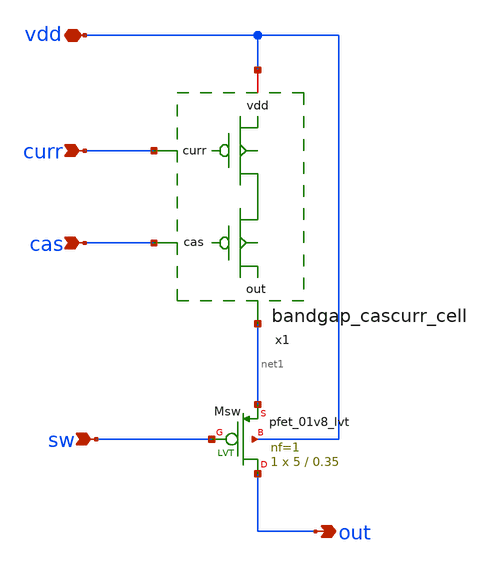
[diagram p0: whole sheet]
** sch_path: design/bandgap_cascurr_cell_sw/bandgap_cascurr_cell_sw.sch
**.subckt bandgap_cascurr_cell_sw vdd curr cas out sw
*.iopin vdd
*.ipin curr
*.ipin cas
*.opin out
*.ipin sw
x1 vdd curr cas net1 bandgap_cascurr_cell m=1
XMsw out sw net1 vdd sky130_fd_pr__pfet_01v8_lvt L=0.35 W=5 nf=1 ad='W * 0.29' as='W * 0.29' pd='2 * (W + 0.29)'
+ ps='2 * (W + 0.29)' nrd='0.29 / W' nrs='0.29 / W' sa=0 sb=0 sd=0 mult=1 m=1
**.ends

* expanding   symbol:  bandgap_cascurr_cell/bandgap_cascurr_cell.sym # of pins=4
** sym_path: design/bandgap_cascurr_cell/bandgap_cascurr_cell.sym
** sch_path: design/bandgap_cascurr_cell/bandgap_cascurr_cell.sch
.subckt bandgap_cascurr_cell vdd curr cas out
*.iopin vdd
*.ipin curr
*.ipin cas
*.opin out
XMcurr net1 curr vdd vdd sky130_fd_pr__pfet_01v8 L=8 W=5 nf=1 ad='W * 0.29' as='W * 0.29' pd='2 * (W + 0.29)'
+ ps='2 * (W + 0.29)' nrd='0.29 / W' nrs='0.29 / W' sa=0 sb=0 sd=0 mult=1 m=1
XMcas out cas net1 vdd sky130_fd_pr__pfet_01v8 L=0.35 W=5 nf=1 ad='W * 0.29' as='W * 0.29' pd='2 * (W + 0.29)'
+ ps='2 * (W + 0.29)' nrd='0.29 / W' nrs='0.29 / W' sa=0 sb=0 sd=0 mult=1 m=1
.ends

.end
